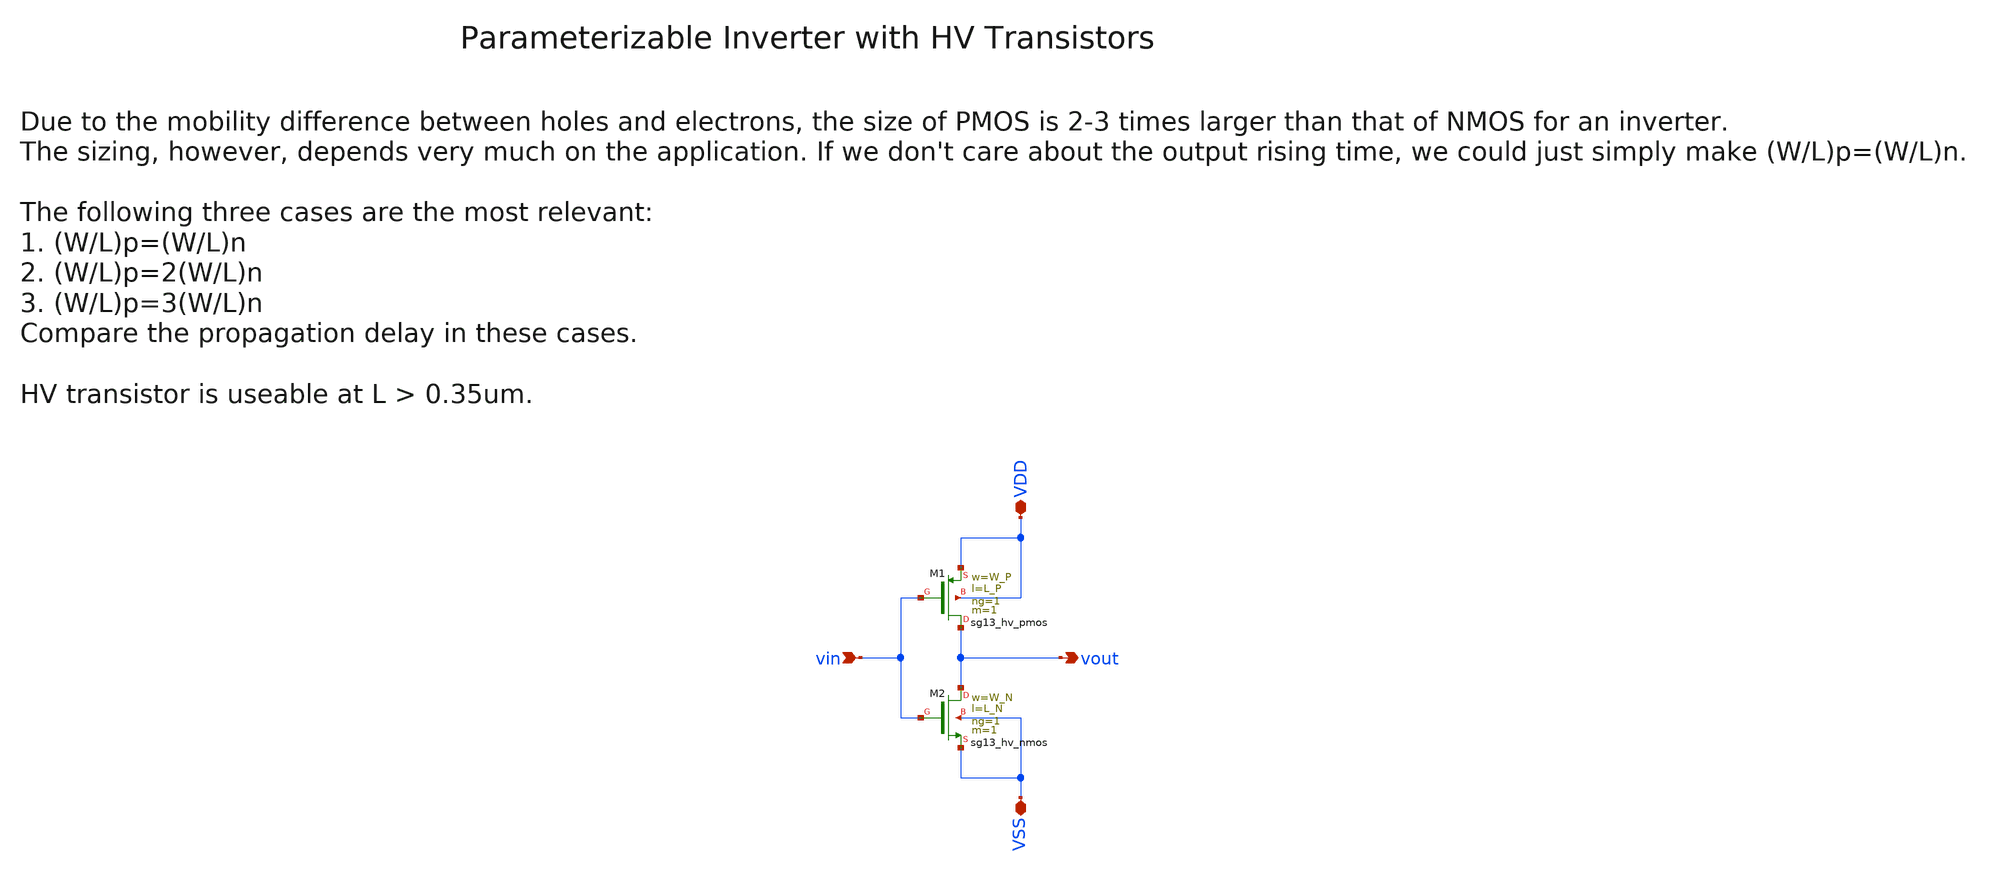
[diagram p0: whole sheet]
** sch_path: SG13G2_ATBS-ADC-main/xschem/inverter/inverter_hv.sch
**.subckt inverter_hv vin VDD VSS vout
*.ipin vin
*.iopin VDD
*.iopin VSS
*.opin vout
XM1 vout vin VDD VDD sg13_hv_pmos w=W_P l=L_P ng=1 m=1 mm_ok=1
XM2 vout vin VSS VSS sg13_hv_nmos w=W_N l=L_N ng=1 m=1 mm_ok=1
**.ends
.end
